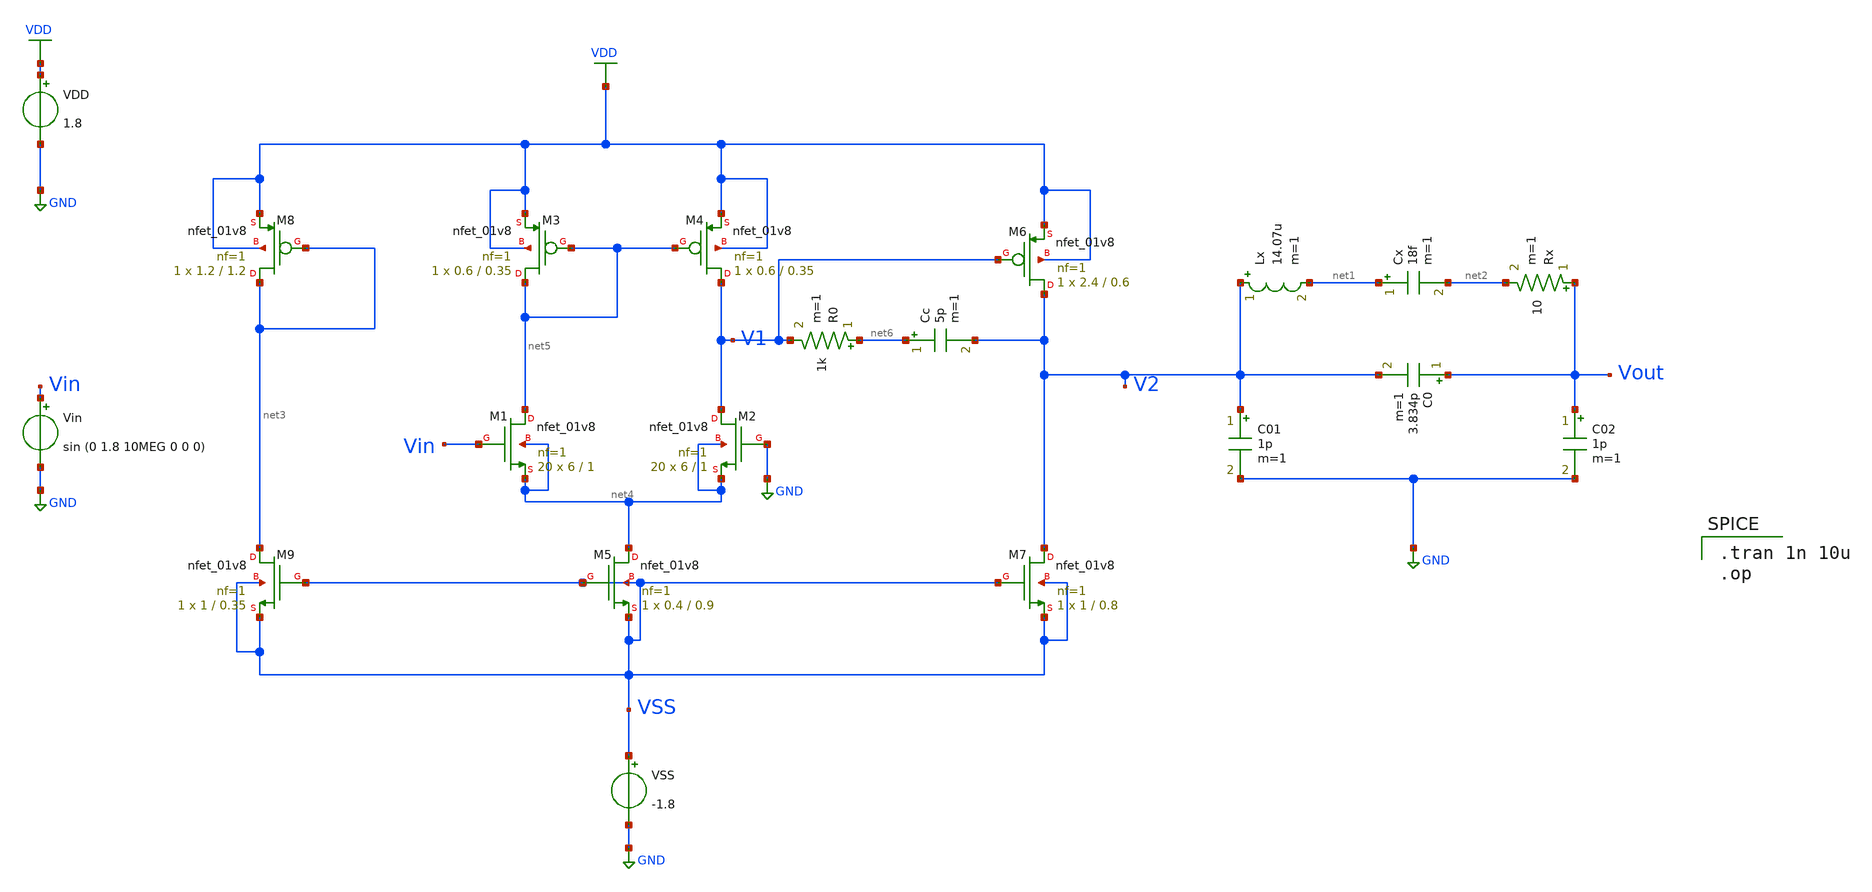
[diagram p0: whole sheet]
** sch_path: pll/xctl_lib/xctl_test/xschem/xctl_test.sch
**.subckt xctl_test
Lx V2 net1 14.07u m=1
Cx net1 net2 18f m=1
Rx Vout net2 10 m=1
C0 Vout V2 3.834p m=1
C02 Vout GND 1p m=1
C01 V2 GND 1p m=1
XM7 V2 VSS VSS VSS sky130_fd_pr__nfet_01v8 L=0.8 W=1 nf=1 ad='int((nf+1)/2) * W/nf * 0.29' as='int((nf+2)/2) * W/nf * 0.29'
+ pd='2*int((nf+1)/2) * (W/nf + 0.29)' ps='2*int((nf+2)/2) * (W/nf + 0.29)' nrd='0.29 / W' nrs='0.29 / W'
+ sa=0 sb=0 sd=0 mult=1 m=1
XM5 net4 VSS VSS VSS sky130_fd_pr__nfet_01v8 L=0.9 W=0.4 nf=1 ad='int((nf+1)/2) * W/nf * 0.29' as='int((nf+2)/2) * W/nf * 0.29'
+ pd='2*int((nf+1)/2) * (W/nf + 0.29)' ps='2*int((nf+2)/2) * (W/nf + 0.29)' nrd='0.29 / W' nrs='0.29 / W'
+ sa=0 sb=0 sd=0 mult=1 m=1
XM9 net3 VSS VSS VSS sky130_fd_pr__nfet_01v8 L=0.35 W=1 nf=1 ad='int((nf+1)/2) * W/nf * 0.29' as='int((nf+2)/2) * W/nf * 0.29'
+ pd='2*int((nf+1)/2) * (W/nf + 0.29)' ps='2*int((nf+2)/2) * (W/nf + 0.29)' nrd='0.29 / W' nrs='0.29 / W'
+ sa=0 sb=0 sd=0 mult=1 m=1
XM6 V2 V1 VDD VDD sky130_fd_pr__nfet_01v8 L=0.6 W=2.4 nf=1 ad='int((nf+1)/2) * W/nf * 0.29' as='int((nf+2)/2) * W/nf * 0.29'
+ pd='2*int((nf+1)/2) * (W/nf + 0.29)' ps='2*int((nf+2)/2) * (W/nf + 0.29)' nrd='0.29 / W' nrs='0.29 / W'
+ sa=0 sb=0 sd=0 mult=1 m=1
XM4 V1 net5 VDD VDD sky130_fd_pr__nfet_01v8 L=0.35 W=0.6 nf=1 ad='int((nf+1)/2) * W/nf * 0.29' as='int((nf+2)/2) * W/nf * 0.29'
+ pd='2*int((nf+1)/2) * (W/nf + 0.29)' ps='2*int((nf+2)/2) * (W/nf + 0.29)' nrd='0.29 / W' nrs='0.29 / W'
+ sa=0 sb=0 sd=0 mult=1 m=1
XM3 net5 net5 VDD VDD sky130_fd_pr__nfet_01v8 L=0.35 W=0.6 nf=1 ad='int((nf+1)/2) * W/nf * 0.29' as='int((nf+2)/2) * W/nf * 0.29'
+ pd='2*int((nf+1)/2) * (W/nf + 0.29)' ps='2*int((nf+2)/2) * (W/nf + 0.29)' nrd='0.29 / W' nrs='0.29 / W'
+ sa=0 sb=0 sd=0 mult=1 m=1
XM8 net3 net3 VDD VDD sky130_fd_pr__nfet_01v8 L=1.2 W=1.2 nf=1 ad='int((nf+1)/2) * W/nf * 0.29' as='int((nf+2)/2) * W/nf * 0.29'
+ pd='2*int((nf+1)/2) * (W/nf + 0.29)' ps='2*int((nf+2)/2) * (W/nf + 0.29)' nrd='0.29 / W' nrs='0.29 / W'
+ sa=0 sb=0 sd=0 mult=1 m=1
XM1 net5 Vin net4 net4 sky130_fd_pr__nfet_01v8 L=1 W=6 nf=1 ad='int((nf+1)/2) * W/nf * 0.29' as='int((nf+2)/2) * W/nf * 0.29'
+ pd='2*int((nf+1)/2) * (W/nf + 0.29)' ps='2*int((nf+2)/2) * (W/nf + 0.29)' nrd='0.29 / W' nrs='0.29 / W'
+ sa=0 sb=0 sd=0 mult=20 m=20
XM2 V1 GND net4 net4 sky130_fd_pr__nfet_01v8 L=1 W=6 nf=1 ad='int((nf+1)/2) * W/nf * 0.29' as='int((nf+2)/2) * W/nf * 0.29'
+ pd='2*int((nf+1)/2) * (W/nf + 0.29)' ps='2*int((nf+2)/2) * (W/nf + 0.29)' nrd='0.29 / W' nrs='0.29 / W'
+ sa=0 sb=0 sd=0 mult=20 m=20
VDD VDD GND 1.8
Vin Vin GND sin (0 1.8 10MEG 0 0 0)
R0 net6 V1 1k m=1
Cc net6 V2 5p m=1
VSS VSS GND -1.8
**** begin user architecture code

.tran 1n 10u
.op


** opencircuitdesign pdks install
.lib $::SKYWATER_MODELS/sky130.lib.spice tt


**** end user architecture code
**.ends
.GLOBAL VDD
.GLOBAL GND
.end
